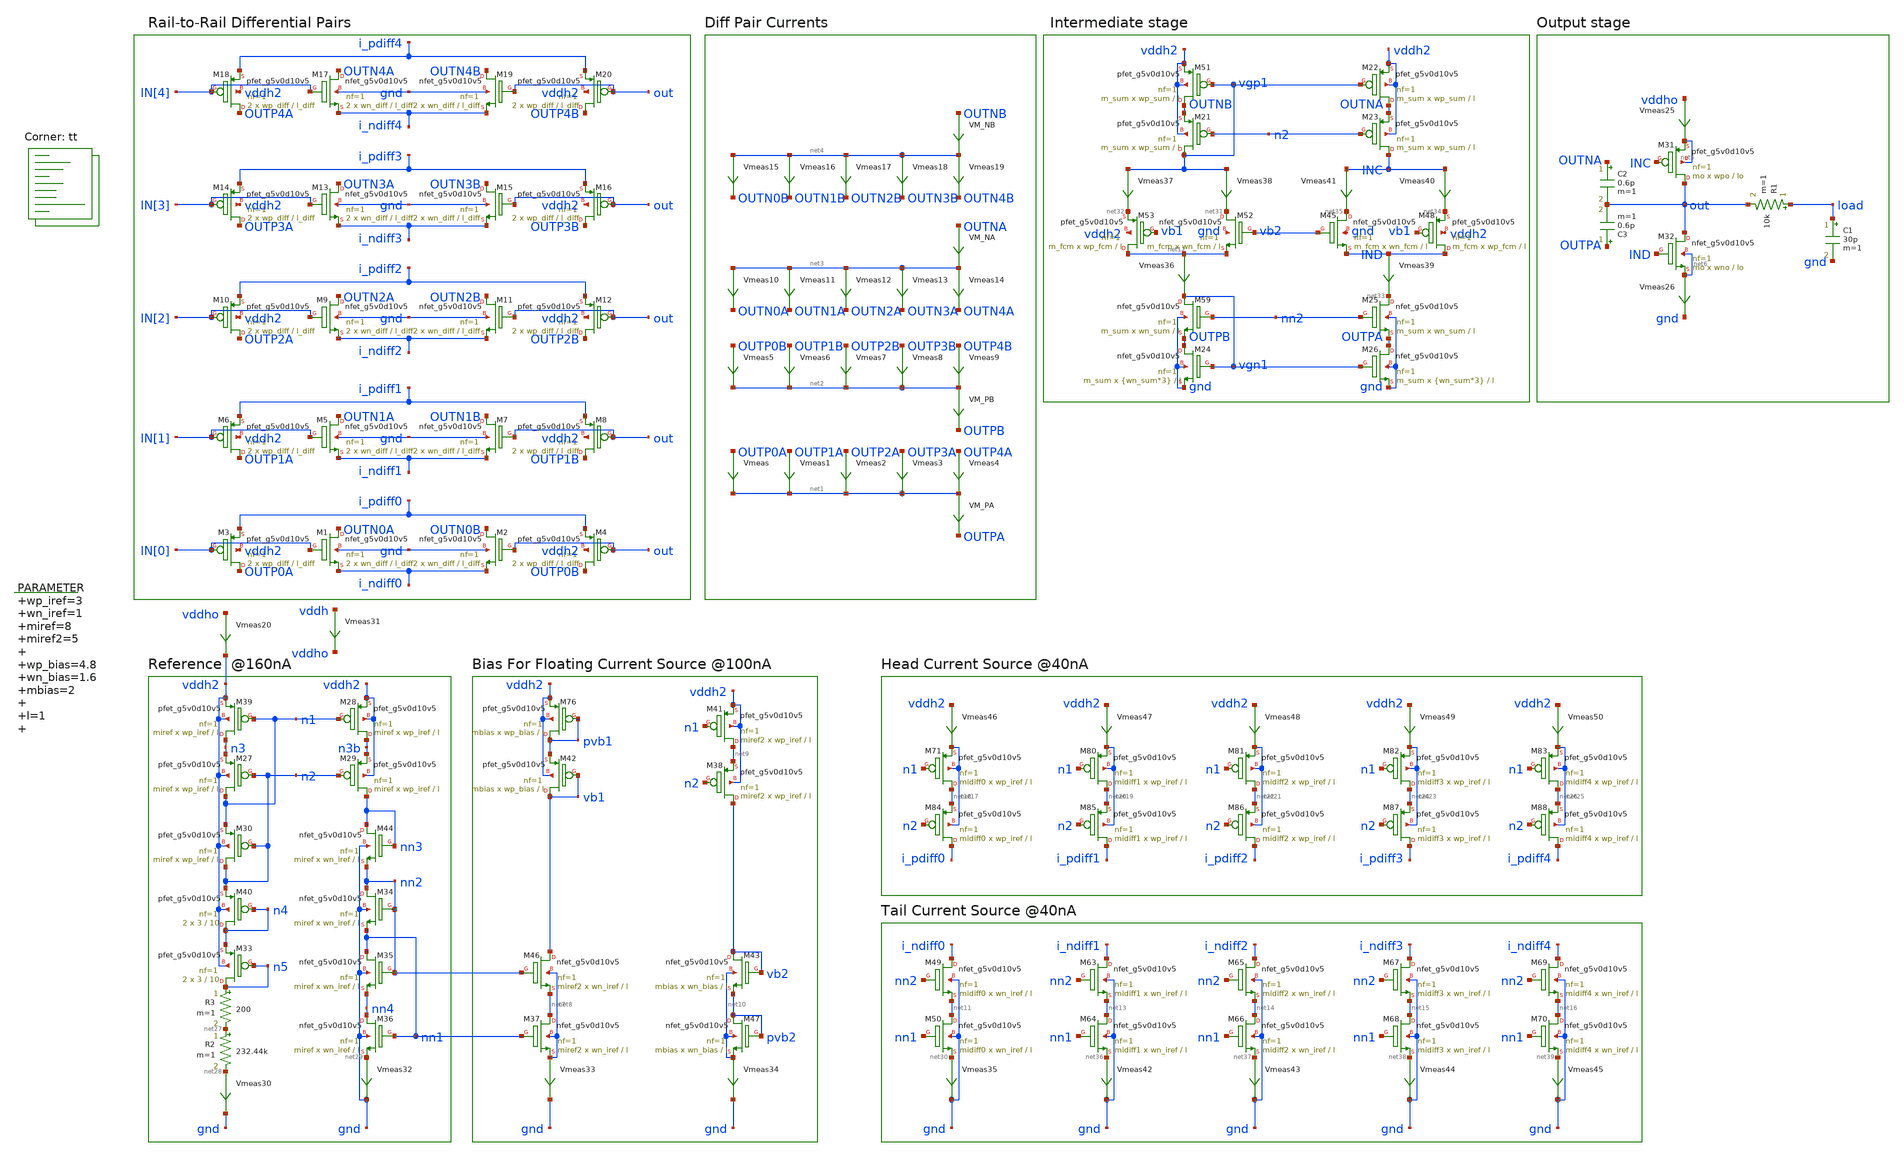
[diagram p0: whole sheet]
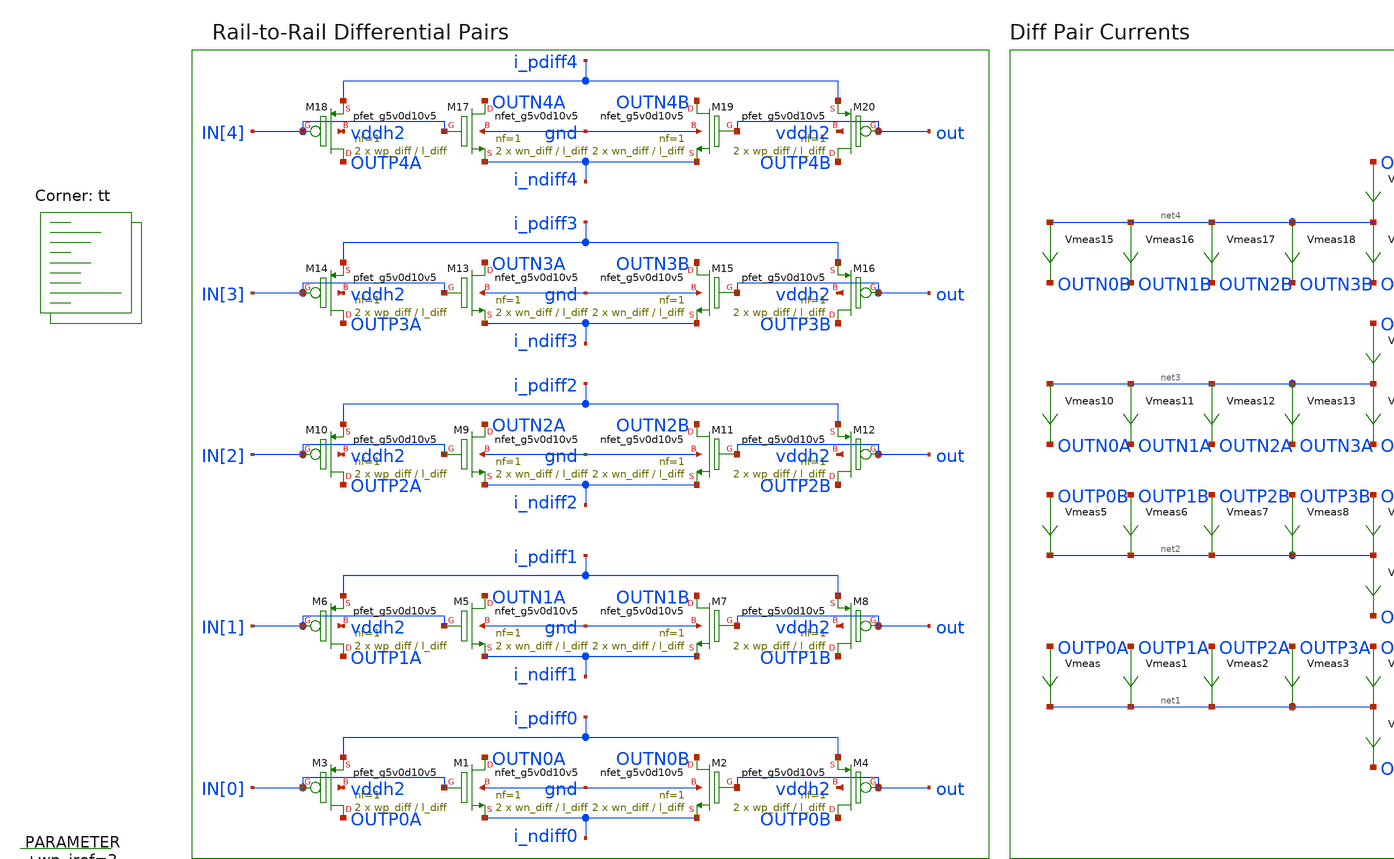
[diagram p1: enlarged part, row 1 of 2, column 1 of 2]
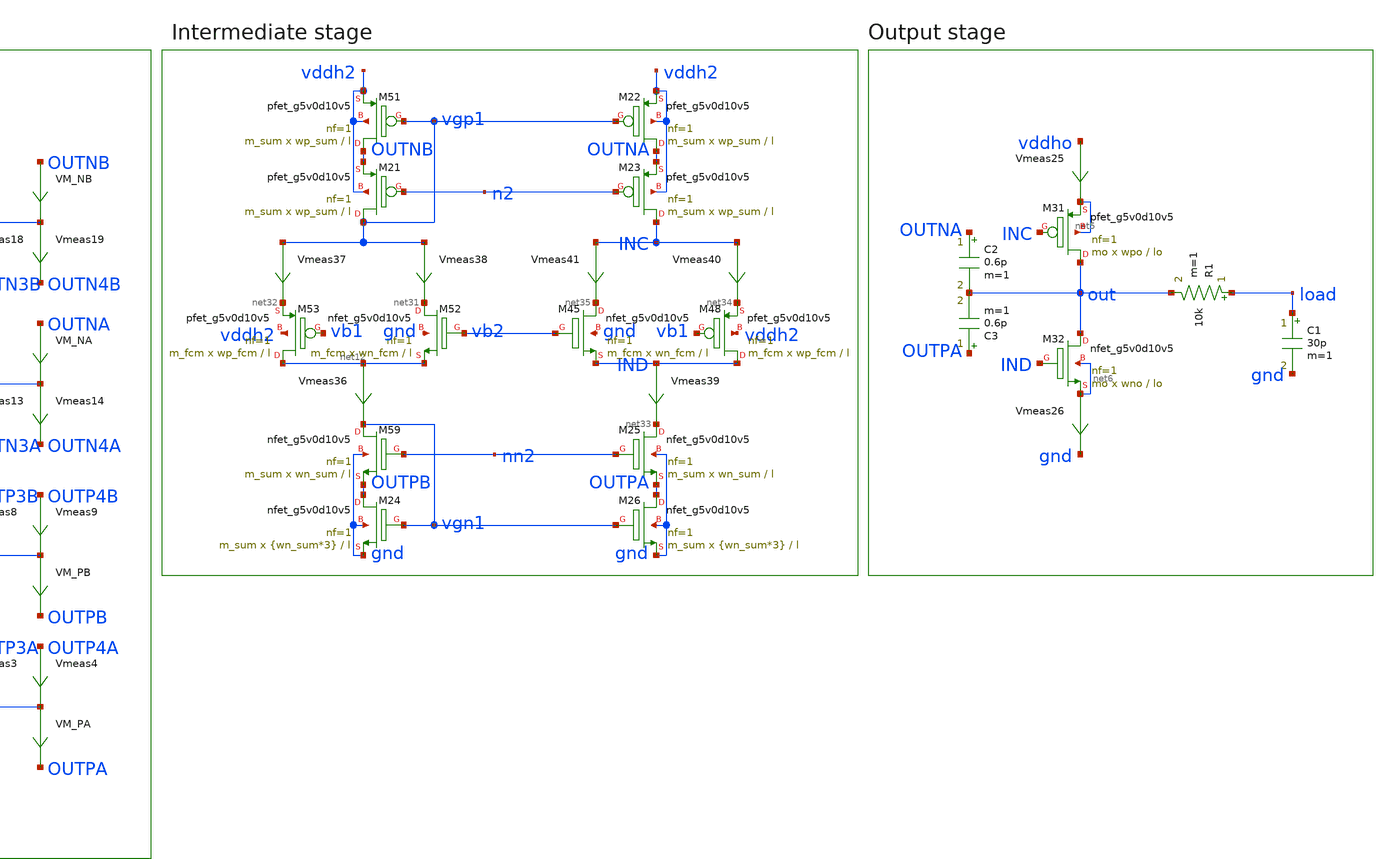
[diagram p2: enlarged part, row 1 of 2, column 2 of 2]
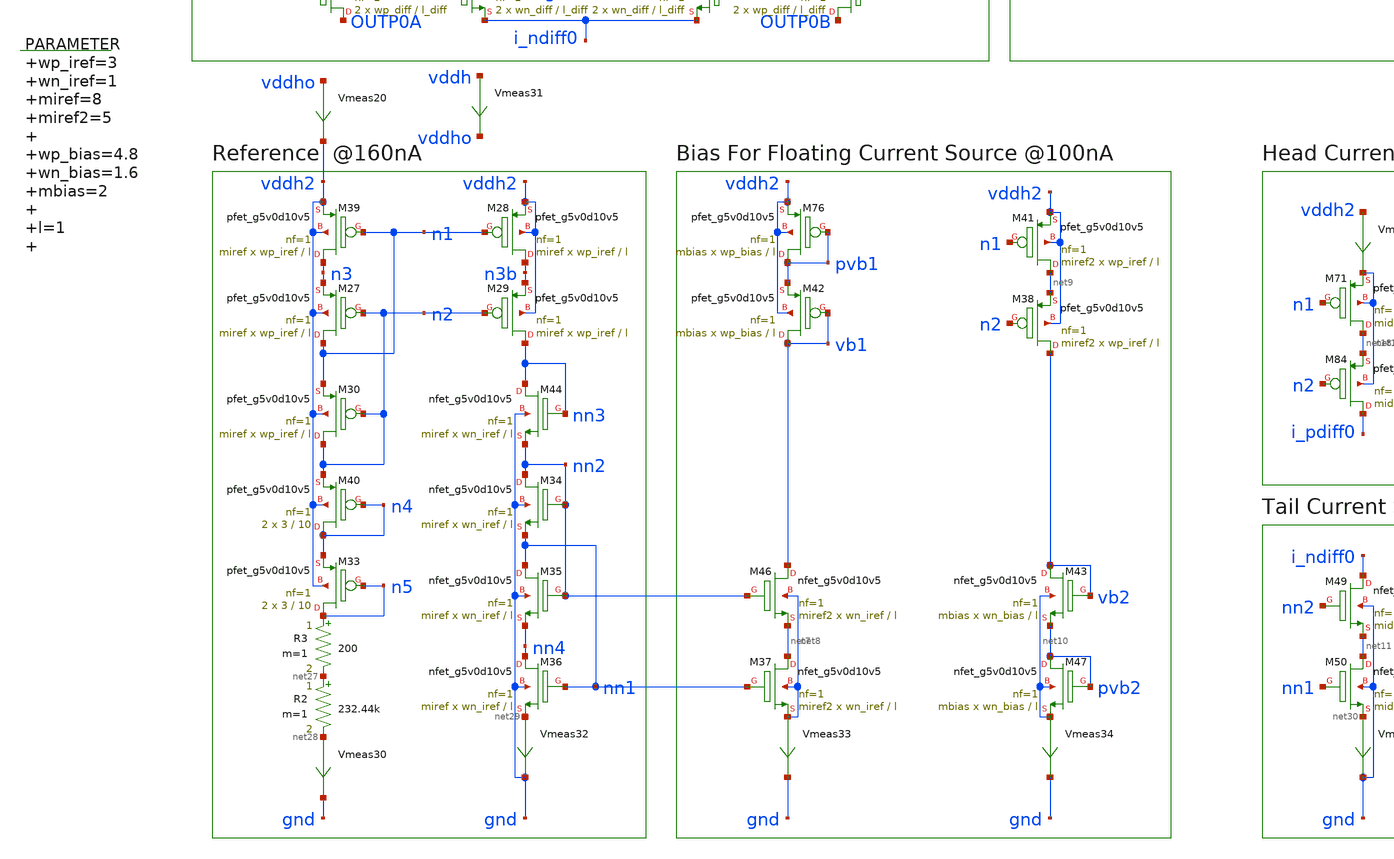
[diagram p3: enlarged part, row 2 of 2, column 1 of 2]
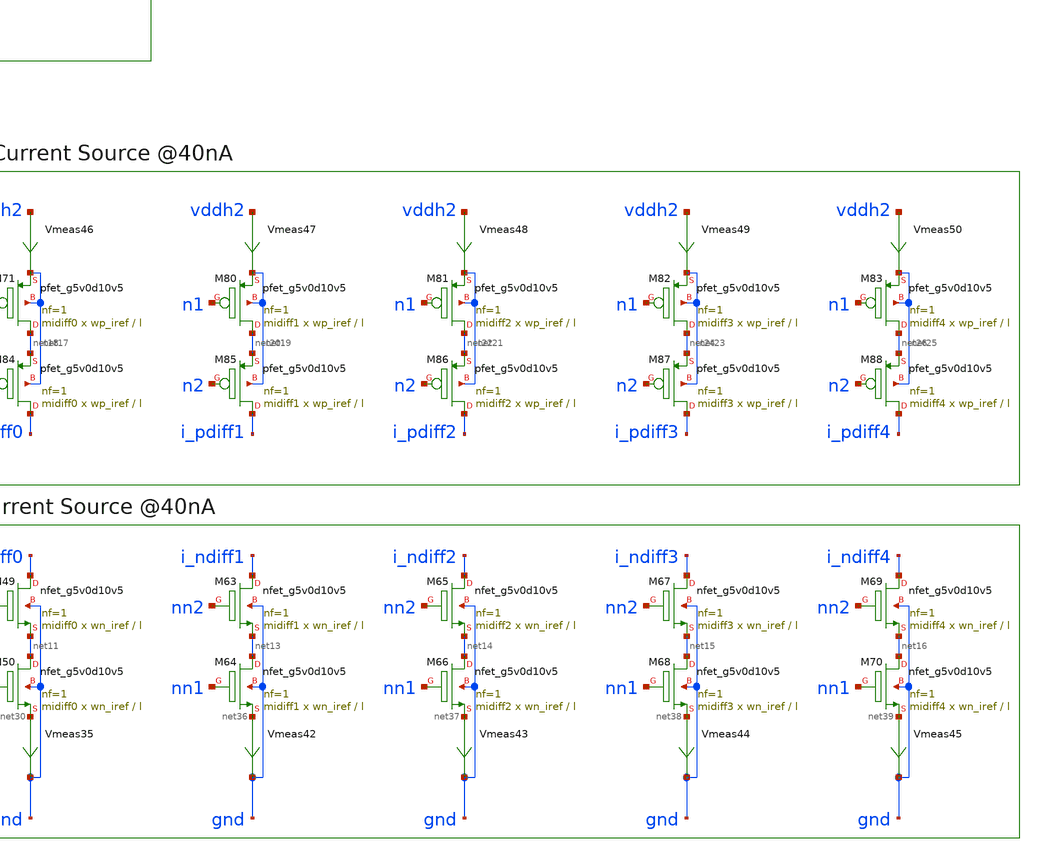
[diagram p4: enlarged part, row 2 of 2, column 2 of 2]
** sch_path: xschem/op_amp_v3-tb.sch
**.subckt op_amp_v3-tb
XM1 OUTN0A IN[0] i_ndiff0 gnd sky130_fd_pr__nfet_g5v0d10v5 L=l_diff W=wn_diff nf=1 ad='int((nf+1)/2) * W/nf * 0.29'
+ as='int((nf+2)/2) * W/nf * 0.29' pd='2*int((nf+1)/2) * (W/nf + 0.29)' ps='2*int((nf+2)/2) * (W/nf + 0.29)'
+ nrd='0.29 / W' nrs='0.29 / W' sa=0 sb=0 sd=0 mult=2 m=2
XM3 OUTP0A IN[0] i_pdiff0 vddh2 sky130_fd_pr__pfet_g5v0d10v5 L=l_diff W=wp_diff nf=1 ad='int((nf+1)/2) * W/nf * 0.29'
+ as='int((nf+2)/2) * W/nf * 0.29' pd='2*int((nf+1)/2) * (W/nf + 0.29)' ps='2*int((nf+2)/2) * (W/nf + 0.29)'
+ nrd='0.29 / W' nrs='0.29 / W' sa=0 sb=0 sd=0 mult=2 m=2
Vmeas OUTP0A net1 0
.save i(vmeas)
Vmeas1 OUTP1A net1 0
.save i(vmeas1)
Vmeas2 OUTP2A net1 0
.save i(vmeas2)
Vmeas3 OUTP3A net1 0
.save i(vmeas3)
Vmeas4 OUTP4A net1 0
.save i(vmeas4)
Vmeas5 OUTP0B net2 0
.save i(vmeas5)
Vmeas6 OUTP1B net2 0
.save i(vmeas6)
Vmeas7 OUTP2B net2 0
.save i(vmeas7)
Vmeas8 OUTP3B net2 0
.save i(vmeas8)
Vmeas9 OUTP4B net2 0
.save i(vmeas9)
Vmeas10 net3 OUTN0A 0
.save i(vmeas10)
Vmeas11 net3 OUTN1A 0
.save i(vmeas11)
Vmeas12 net3 OUTN2A 0
.save i(vmeas12)
Vmeas13 net3 OUTN3A 0
.save i(vmeas13)
Vmeas14 net3 OUTN4A 0
.save i(vmeas14)
Vmeas15 net4 OUTN0B 0
.save i(vmeas15)
Vmeas16 net4 OUTN1B 0
.save i(vmeas16)
Vmeas17 net4 OUTN2B 0
.save i(vmeas17)
Vmeas18 net4 OUTN3B 0
.save i(vmeas18)
Vmeas19 net4 OUTN4B 0
.save i(vmeas19)
XM31 out INC net5 net5 sky130_fd_pr__pfet_g5v0d10v5 L=lo W=wpo nf=1 ad='int((nf+1)/2) * W/nf * 0.29'
+ as='int((nf+2)/2) * W/nf * 0.29' pd='2*int((nf+1)/2) * (W/nf + 0.29)' ps='2*int((nf+2)/2) * (W/nf + 0.29)'
+ nrd='0.29 / W' nrs='0.29 / W' sa=0 sb=0 sd=0 mult=mo m=mo
XM32 out IND net6 net6 sky130_fd_pr__nfet_g5v0d10v5 L=lo W=wno nf=1 ad='int((nf+1)/2) * W/nf * 0.29'
+ as='int((nf+2)/2) * W/nf * 0.29' pd='2*int((nf+1)/2) * (W/nf + 0.29)' ps='2*int((nf+2)/2) * (W/nf + 0.29)'
+ nrd='0.29 / W' nrs='0.29 / W' sa=0 sb=0 sd=0 mult=mo m=mo
R1 load out 10k m=1
Vmeas25 vddho net5 0
.save i(vmeas25)
Vmeas26 net6 gnd 0
.save i(vmeas26)
C1 load gnd 30p m=1
VM_NB OUTNB net4 0
.save i(vm_nb)
VM_NA OUTNA net3 0
.save i(vm_na)
VM_PB net2 OUTPB 0
.save i(vm_pb)
VM_PA net1 OUTPA 0
.save i(vm_pa)
C2 OUTNA out 0.6p m=1
C3 OUTPA out 0.6p m=1
XM2 OUTN0B out i_ndiff0 gnd sky130_fd_pr__nfet_g5v0d10v5 L=l_diff W=wn_diff nf=1 ad='int((nf+1)/2) * W/nf * 0.29'
+ as='int((nf+2)/2) * W/nf * 0.29' pd='2*int((nf+1)/2) * (W/nf + 0.29)' ps='2*int((nf+2)/2) * (W/nf + 0.29)'
+ nrd='0.29 / W' nrs='0.29 / W' sa=0 sb=0 sd=0 mult=2 m=2
XM4 OUTP0B out i_pdiff0 vddh2 sky130_fd_pr__pfet_g5v0d10v5 L=l_diff W=wp_diff nf=1 ad='int((nf+1)/2) * W/nf * 0.29'
+ as='int((nf+2)/2) * W/nf * 0.29' pd='2*int((nf+1)/2) * (W/nf + 0.29)' ps='2*int((nf+2)/2) * (W/nf + 0.29)'
+ nrd='0.29 / W' nrs='0.29 / W' sa=0 sb=0 sd=0 mult=2 m=2
XM5 OUTN1A IN[1] i_ndiff1 gnd sky130_fd_pr__nfet_g5v0d10v5 L=l_diff W=wn_diff nf=1 ad='int((nf+1)/2) * W/nf * 0.29'
+ as='int((nf+2)/2) * W/nf * 0.29' pd='2*int((nf+1)/2) * (W/nf + 0.29)' ps='2*int((nf+2)/2) * (W/nf + 0.29)'
+ nrd='0.29 / W' nrs='0.29 / W' sa=0 sb=0 sd=0 mult=2 m=2
XM6 OUTP1A IN[1] i_pdiff1 vddh2 sky130_fd_pr__pfet_g5v0d10v5 L=l_diff W=wp_diff nf=1 ad='int((nf+1)/2) * W/nf * 0.29'
+ as='int((nf+2)/2) * W/nf * 0.29' pd='2*int((nf+1)/2) * (W/nf + 0.29)' ps='2*int((nf+2)/2) * (W/nf + 0.29)'
+ nrd='0.29 / W' nrs='0.29 / W' sa=0 sb=0 sd=0 mult=2 m=2
XM7 OUTN1B out i_ndiff1 gnd sky130_fd_pr__nfet_g5v0d10v5 L=l_diff W=wn_diff nf=1 ad='int((nf+1)/2) * W/nf * 0.29'
+ as='int((nf+2)/2) * W/nf * 0.29' pd='2*int((nf+1)/2) * (W/nf + 0.29)' ps='2*int((nf+2)/2) * (W/nf + 0.29)'
+ nrd='0.29 / W' nrs='0.29 / W' sa=0 sb=0 sd=0 mult=2 m=2
XM8 OUTP1B out i_pdiff1 vddh2 sky130_fd_pr__pfet_g5v0d10v5 L=l_diff W=wp_diff nf=1 ad='int((nf+1)/2) * W/nf * 0.29'
+ as='int((nf+2)/2) * W/nf * 0.29' pd='2*int((nf+1)/2) * (W/nf + 0.29)' ps='2*int((nf+2)/2) * (W/nf + 0.29)'
+ nrd='0.29 / W' nrs='0.29 / W' sa=0 sb=0 sd=0 mult=2 m=2
XM9 OUTN2A IN[2] i_ndiff2 gnd sky130_fd_pr__nfet_g5v0d10v5 L=l_diff W=wn_diff nf=1 ad='int((nf+1)/2) * W/nf * 0.29'
+ as='int((nf+2)/2) * W/nf * 0.29' pd='2*int((nf+1)/2) * (W/nf + 0.29)' ps='2*int((nf+2)/2) * (W/nf + 0.29)'
+ nrd='0.29 / W' nrs='0.29 / W' sa=0 sb=0 sd=0 mult=2 m=2
XM10 OUTP2A IN[2] i_pdiff2 vddh2 sky130_fd_pr__pfet_g5v0d10v5 L=l_diff W=wp_diff nf=1 ad='int((nf+1)/2) * W/nf * 0.29'
+ as='int((nf+2)/2) * W/nf * 0.29' pd='2*int((nf+1)/2) * (W/nf + 0.29)' ps='2*int((nf+2)/2) * (W/nf + 0.29)'
+ nrd='0.29 / W' nrs='0.29 / W' sa=0 sb=0 sd=0 mult=2 m=2
XM11 OUTN2B out i_ndiff2 gnd sky130_fd_pr__nfet_g5v0d10v5 L=l_diff W=wn_diff nf=1 ad='int((nf+1)/2) * W/nf * 0.29'
+ as='int((nf+2)/2) * W/nf * 0.29' pd='2*int((nf+1)/2) * (W/nf + 0.29)' ps='2*int((nf+2)/2) * (W/nf + 0.29)'
+ nrd='0.29 / W' nrs='0.29 / W' sa=0 sb=0 sd=0 mult=2 m=2
XM12 OUTP2B out i_pdiff2 vddh2 sky130_fd_pr__pfet_g5v0d10v5 L=l_diff W=wp_diff nf=1 ad='int((nf+1)/2) * W/nf * 0.29'
+ as='int((nf+2)/2) * W/nf * 0.29' pd='2*int((nf+1)/2) * (W/nf + 0.29)' ps='2*int((nf+2)/2) * (W/nf + 0.29)'
+ nrd='0.29 / W' nrs='0.29 / W' sa=0 sb=0 sd=0 mult=2 m=2
XM13 OUTN3A IN[3] i_ndiff3 gnd sky130_fd_pr__nfet_g5v0d10v5 L=l_diff W=wn_diff nf=1 ad='int((nf+1)/2) * W/nf * 0.29'
+ as='int((nf+2)/2) * W/nf * 0.29' pd='2*int((nf+1)/2) * (W/nf + 0.29)' ps='2*int((nf+2)/2) * (W/nf + 0.29)'
+ nrd='0.29 / W' nrs='0.29 / W' sa=0 sb=0 sd=0 mult=2 m=2
XM14 OUTP3A IN[3] i_pdiff3 vddh2 sky130_fd_pr__pfet_g5v0d10v5 L=l_diff W=wp_diff nf=1 ad='int((nf+1)/2) * W/nf * 0.29'
+ as='int((nf+2)/2) * W/nf * 0.29' pd='2*int((nf+1)/2) * (W/nf + 0.29)' ps='2*int((nf+2)/2) * (W/nf + 0.29)'
+ nrd='0.29 / W' nrs='0.29 / W' sa=0 sb=0 sd=0 mult=2 m=2
XM15 OUTN3B out i_ndiff3 gnd sky130_fd_pr__nfet_g5v0d10v5 L=l_diff W=wn_diff nf=1 ad='int((nf+1)/2) * W/nf * 0.29'
+ as='int((nf+2)/2) * W/nf * 0.29' pd='2*int((nf+1)/2) * (W/nf + 0.29)' ps='2*int((nf+2)/2) * (W/nf + 0.29)'
+ nrd='0.29 / W' nrs='0.29 / W' sa=0 sb=0 sd=0 mult=2 m=2
XM16 OUTP3B out i_pdiff3 vddh2 sky130_fd_pr__pfet_g5v0d10v5 L=l_diff W=wp_diff nf=1 ad='int((nf+1)/2) * W/nf * 0.29'
+ as='int((nf+2)/2) * W/nf * 0.29' pd='2*int((nf+1)/2) * (W/nf + 0.29)' ps='2*int((nf+2)/2) * (W/nf + 0.29)'
+ nrd='0.29 / W' nrs='0.29 / W' sa=0 sb=0 sd=0 mult=2 m=2
XM17 OUTN4A IN[4] i_ndiff4 gnd sky130_fd_pr__nfet_g5v0d10v5 L=l_diff W=wn_diff nf=1 ad='int((nf+1)/2) * W/nf * 0.29'
+ as='int((nf+2)/2) * W/nf * 0.29' pd='2*int((nf+1)/2) * (W/nf + 0.29)' ps='2*int((nf+2)/2) * (W/nf + 0.29)'
+ nrd='0.29 / W' nrs='0.29 / W' sa=0 sb=0 sd=0 mult=2 m=2
XM18 OUTP4A IN[4] i_pdiff4 vddh2 sky130_fd_pr__pfet_g5v0d10v5 L=l_diff W=wp_diff nf=1 ad='int((nf+1)/2) * W/nf * 0.29'
+ as='int((nf+2)/2) * W/nf * 0.29' pd='2*int((nf+1)/2) * (W/nf + 0.29)' ps='2*int((nf+2)/2) * (W/nf + 0.29)'
+ nrd='0.29 / W' nrs='0.29 / W' sa=0 sb=0 sd=0 mult=2 m=2
XM19 OUTN4B out i_ndiff4 gnd sky130_fd_pr__nfet_g5v0d10v5 L=l_diff W=wn_diff nf=1 ad='int((nf+1)/2) * W/nf * 0.29'
+ as='int((nf+2)/2) * W/nf * 0.29' pd='2*int((nf+1)/2) * (W/nf + 0.29)' ps='2*int((nf+2)/2) * (W/nf + 0.29)'
+ nrd='0.29 / W' nrs='0.29 / W' sa=0 sb=0 sd=0 mult=2 m=2
XM20 OUTP4B out i_pdiff4 vddh2 sky130_fd_pr__pfet_g5v0d10v5 L=l_diff W=wp_diff nf=1 ad='int((nf+1)/2) * W/nf * 0.29'
+ as='int((nf+2)/2) * W/nf * 0.29' pd='2*int((nf+1)/2) * (W/nf + 0.29)' ps='2*int((nf+2)/2) * (W/nf + 0.29)'
+ nrd='0.29 / W' nrs='0.29 / W' sa=0 sb=0 sd=0 mult=2 m=2
XM39 n3 n1 vddh2 vddh2 sky130_fd_pr__pfet_g5v0d10v5 L=l W=wp_iref nf=1 ad='int((nf+1)/2) * W/nf * 0.29'
+ as='int((nf+2)/2) * W/nf * 0.29' pd='2*int((nf+1)/2) * (W/nf + 0.29)' ps='2*int((nf+2)/2) * (W/nf + 0.29)'
+ nrd='0.29 / W' nrs='0.29 / W' sa=0 sb=0 sd=0 mult=miref m=miref
R2 net27 net28 232.44k m=1
Vmeas30 net28 gnd 0
.save i(vmeas30)
R3 n5 net27 200 m=1
XM40 n4 n4 n2 vddh2 sky130_fd_pr__pfet_g5v0d10v5 L=10 W=3 nf=1 ad='int((nf+1)/2) * W/nf * 0.29' as='int((nf+2)/2) * W/nf * 0.29'
+ pd='2*int((nf+1)/2) * (W/nf + 0.29)' ps='2*int((nf+2)/2) * (W/nf + 0.29)' nrd='0.29 / W' nrs='0.29 / W'
+ sa=0 sb=0 sd=0 mult=2 m=2
Vmeas31 vddh vddho 0
.save i(vmeas31)
XM44 nn3 nn3 nn2 gnd sky130_fd_pr__nfet_g5v0d10v5 L=l W=wn_iref nf=1 ad='int((nf+1)/2) * W/nf * 0.29'
+ as='int((nf+2)/2) * W/nf * 0.29' pd='2*int((nf+1)/2) * (W/nf + 0.29)' ps='2*int((nf+2)/2) * (W/nf + 0.29)'
+ nrd='0.29 / W' nrs='0.29 / W' sa=0 sb=0 sd=0 mult=miref m=miref
Vmeas32 net29 gnd 0
.save i(vmeas32)
XM46 vb1 nn2 net7 net8 sky130_fd_pr__nfet_g5v0d10v5 L=l W=wn_iref nf=1 ad='int((nf+1)/2) * W/nf * 0.29'
+ as='int((nf+2)/2) * W/nf * 0.29' pd='2*int((nf+1)/2) * (W/nf + 0.29)' ps='2*int((nf+2)/2) * (W/nf + 0.29)'
+ nrd='0.29 / W' nrs='0.29 / W' sa=0 sb=0 sd=0 mult=miref2 m=miref2
Vmeas33 net8 gnd 0
.save i(vmeas33)
XM47 pvb2 pvb2 net10 net10 sky130_fd_pr__nfet_g5v0d10v5 L=l W=wn_bias nf=1 ad='int((nf+1)/2) * W/nf * 0.29'
+ as='int((nf+2)/2) * W/nf * 0.29' pd='2*int((nf+1)/2) * (W/nf + 0.29)' ps='2*int((nf+2)/2) * (W/nf + 0.29)'
+ nrd='0.29 / W' nrs='0.29 / W' sa=0 sb=0 sd=0 mult=mbias m=mbias
Vmeas34 net10 gnd 0
.save i(vmeas34)
XM49 i_ndiff0 nn2 net11 gnd sky130_fd_pr__nfet_g5v0d10v5 L=l W=wn_iref nf=1 ad='int((nf+1)/2) * W/nf * 0.29'
+ as='int((nf+2)/2) * W/nf * 0.29' pd='2*int((nf+1)/2) * (W/nf + 0.29)' ps='2*int((nf+2)/2) * (W/nf + 0.29)'
+ nrd='0.29 / W' nrs='0.29 / W' sa=0 sb=0 sd=0 mult=midiff0 m=midiff0
XM50 net11 nn1 net30 gnd sky130_fd_pr__nfet_g5v0d10v5 L=l W=wn_iref nf=1 ad='int((nf+1)/2) * W/nf * 0.29'
+ as='int((nf+2)/2) * W/nf * 0.29' pd='2*int((nf+1)/2) * (W/nf + 0.29)' ps='2*int((nf+2)/2) * (W/nf + 0.29)'
+ nrd='0.29 / W' nrs='0.29 / W' sa=0 sb=0 sd=0 mult=midiff0 m=midiff0
Vmeas35 net30 gnd 0
.save i(vmeas35)
Vmeas36 net12 vgn1 0
.save i(vmeas36)
XM51 OUTNB vgp1 vddh2 vddh2 sky130_fd_pr__pfet_g5v0d10v5 L=l W=wp_sum nf=1 ad='int((nf+1)/2) * W/nf * 0.29'
+ as='int((nf+2)/2) * W/nf * 0.29' pd='2*int((nf+1)/2) * (W/nf + 0.29)' ps='2*int((nf+2)/2) * (W/nf + 0.29)'
+ nrd='0.29 / W' nrs='0.29 / W' sa=0 sb=0 sd=0 mult=m_sum m=m_sum
XM52 net31 vb2 net12 gnd sky130_fd_pr__nfet_g5v0d10v5 L=l W=wn_fcm nf=1 ad='int((nf+1)/2) * W/nf * 0.29'
+ as='int((nf+2)/2) * W/nf * 0.29' pd='2*int((nf+1)/2) * (W/nf + 0.29)' ps='2*int((nf+2)/2) * (W/nf + 0.29)'
+ nrd='0.29 / W' nrs='0.29 / W' sa=0 sb=0 sd=0 mult=m_fcm m=m_fcm
Vmeas37 vgp1 net32 0
.save i(vmeas37)
Vmeas38 vgp1 net31 0
.save i(vmeas38)
XM53 net12 vb1 net32 vddh2 sky130_fd_pr__pfet_g5v0d10v5 L=l W=wp_fcm nf=1 ad='int((nf+1)/2) * W/nf * 0.29'
+ as='int((nf+2)/2) * W/nf * 0.29' pd='2*int((nf+1)/2) * (W/nf + 0.29)' ps='2*int((nf+2)/2) * (W/nf + 0.29)'
+ nrd='0.29 / W' nrs='0.29 / W' sa=0 sb=0 sd=0 mult=m_fcm m=m_fcm
Vmeas39 IND net33 0
.save i(vmeas39)
Vmeas40 INC net34 0
.save i(vmeas40)
Vmeas41 INC net35 0
.save i(vmeas41)
XM59 vgn1 nn2 OUTPB gnd sky130_fd_pr__nfet_g5v0d10v5 L=l W=wn_sum nf=1 ad='int((nf+1)/2) * W/nf * 0.29'
+ as='int((nf+2)/2) * W/nf * 0.29' pd='2*int((nf+1)/2) * (W/nf + 0.29)' ps='2*int((nf+2)/2) * (W/nf + 0.29)'
+ nrd='0.29 / W' nrs='0.29 / W' sa=0 sb=0 sd=0 mult=m_sum m=m_sum
XM63 i_ndiff1 nn2 net13 gnd sky130_fd_pr__nfet_g5v0d10v5 L=l W=wn_iref nf=1 ad='int((nf+1)/2) * W/nf * 0.29'
+ as='int((nf+2)/2) * W/nf * 0.29' pd='2*int((nf+1)/2) * (W/nf + 0.29)' ps='2*int((nf+2)/2) * (W/nf + 0.29)'
+ nrd='0.29 / W' nrs='0.29 / W' sa=0 sb=0 sd=0 mult=midiff1 m=midiff1
XM64 net13 nn1 net36 gnd sky130_fd_pr__nfet_g5v0d10v5 L=l W=wn_iref nf=1 ad='int((nf+1)/2) * W/nf * 0.29'
+ as='int((nf+2)/2) * W/nf * 0.29' pd='2*int((nf+1)/2) * (W/nf + 0.29)' ps='2*int((nf+2)/2) * (W/nf + 0.29)'
+ nrd='0.29 / W' nrs='0.29 / W' sa=0 sb=0 sd=0 mult=midiff1 m=midiff1
Vmeas42 net36 gnd 0
.save i(vmeas42)
XM65 i_ndiff2 nn2 net14 gnd sky130_fd_pr__nfet_g5v0d10v5 L=l W=wn_iref nf=1 ad='int((nf+1)/2) * W/nf * 0.29'
+ as='int((nf+2)/2) * W/nf * 0.29' pd='2*int((nf+1)/2) * (W/nf + 0.29)' ps='2*int((nf+2)/2) * (W/nf + 0.29)'
+ nrd='0.29 / W' nrs='0.29 / W' sa=0 sb=0 sd=0 mult=midiff2 m=midiff2
XM66 net14 nn1 net37 gnd sky130_fd_pr__nfet_g5v0d10v5 L=l W=wn_iref nf=1 ad='int((nf+1)/2) * W/nf * 0.29'
+ as='int((nf+2)/2) * W/nf * 0.29' pd='2*int((nf+1)/2) * (W/nf + 0.29)' ps='2*int((nf+2)/2) * (W/nf + 0.29)'
+ nrd='0.29 / W' nrs='0.29 / W' sa=0 sb=0 sd=0 mult=midiff2 m=midiff2
Vmeas43 net37 gnd 0
.save i(vmeas43)
XM67 i_ndiff3 nn2 net15 gnd sky130_fd_pr__nfet_g5v0d10v5 L=l W=wn_iref nf=1 ad='int((nf+1)/2) * W/nf * 0.29'
+ as='int((nf+2)/2) * W/nf * 0.29' pd='2*int((nf+1)/2) * (W/nf + 0.29)' ps='2*int((nf+2)/2) * (W/nf + 0.29)'
+ nrd='0.29 / W' nrs='0.29 / W' sa=0 sb=0 sd=0 mult=midiff3 m=midiff3
XM68 net15 nn1 net38 gnd sky130_fd_pr__nfet_g5v0d10v5 L=l W=wn_iref nf=1 ad='int((nf+1)/2) * W/nf * 0.29'
+ as='int((nf+2)/2) * W/nf * 0.29' pd='2*int((nf+1)/2) * (W/nf + 0.29)' ps='2*int((nf+2)/2) * (W/nf + 0.29)'
+ nrd='0.29 / W' nrs='0.29 / W' sa=0 sb=0 sd=0 mult=midiff3 m=midiff3
Vmeas44 net38 gnd 0
.save i(vmeas44)
XM69 i_ndiff4 nn2 net16 gnd sky130_fd_pr__nfet_g5v0d10v5 L=l W=wn_iref nf=1 ad='int((nf+1)/2) * W/nf * 0.29'
+ as='int((nf+2)/2) * W/nf * 0.29' pd='2*int((nf+1)/2) * (W/nf + 0.29)' ps='2*int((nf+2)/2) * (W/nf + 0.29)'
+ nrd='0.29 / W' nrs='0.29 / W' sa=0 sb=0 sd=0 mult=midiff4 m=midiff4
XM70 net16 nn1 net39 gnd sky130_fd_pr__nfet_g5v0d10v5 L=l W=wn_iref nf=1 ad='int((nf+1)/2) * W/nf * 0.29'
+ as='int((nf+2)/2) * W/nf * 0.29' pd='2*int((nf+1)/2) * (W/nf + 0.29)' ps='2*int((nf+2)/2) * (W/nf + 0.29)'
+ nrd='0.29 / W' nrs='0.29 / W' sa=0 sb=0 sd=0 mult=midiff4 m=midiff4
Vmeas45 net39 gnd 0
.save i(vmeas45)
XM71 net18 n1 net17 net17 sky130_fd_pr__pfet_g5v0d10v5 L=l W=wp_iref nf=1 ad='int((nf+1)/2) * W/nf * 0.29'
+ as='int((nf+2)/2) * W/nf * 0.29' pd='2*int((nf+1)/2) * (W/nf + 0.29)' ps='2*int((nf+2)/2) * (W/nf + 0.29)'
+ nrd='0.29 / W' nrs='0.29 / W' sa=0 sb=0 sd=0 mult=midiff0 m=midiff0
Vmeas46 vddh2 net17 0
.save i(vmeas46)
XM76 pvb1 pvb1 vddh2 vddh2 sky130_fd_pr__pfet_g5v0d10v5 L=l W=wp_bias nf=1 ad='int((nf+1)/2) * W/nf * 0.29'
+ as='int((nf+2)/2) * W/nf * 0.29' pd='2*int((nf+1)/2) * (W/nf + 0.29)' ps='2*int((nf+2)/2) * (W/nf + 0.29)'
+ nrd='0.29 / W' nrs='0.29 / W' sa=0 sb=0 sd=0 mult=mbias m=mbias
XM80 net20 n1 net19 net19 sky130_fd_pr__pfet_g5v0d10v5 L=l W=wp_iref nf=1 ad='int((nf+1)/2) * W/nf * 0.29'
+ as='int((nf+2)/2) * W/nf * 0.29' pd='2*int((nf+1)/2) * (W/nf + 0.29)' ps='2*int((nf+2)/2) * (W/nf + 0.29)'
+ nrd='0.29 / W' nrs='0.29 / W' sa=0 sb=0 sd=0 mult=midiff1 m=midiff1
Vmeas47 vddh2 net19 0
.save i(vmeas47)
XM81 net22 n1 net21 net21 sky130_fd_pr__pfet_g5v0d10v5 L=l W=wp_iref nf=1 ad='int((nf+1)/2) * W/nf * 0.29'
+ as='int((nf+2)/2) * W/nf * 0.29' pd='2*int((nf+1)/2) * (W/nf + 0.29)' ps='2*int((nf+2)/2) * (W/nf + 0.29)'
+ nrd='0.29 / W' nrs='0.29 / W' sa=0 sb=0 sd=0 mult=midiff2 m=midiff2
Vmeas48 vddh2 net21 0
.save i(vmeas48)
XM82 net24 n1 net23 net23 sky130_fd_pr__pfet_g5v0d10v5 L=l W=wp_iref nf=1 ad='int((nf+1)/2) * W/nf * 0.29'
+ as='int((nf+2)/2) * W/nf * 0.29' pd='2*int((nf+1)/2) * (W/nf + 0.29)' ps='2*int((nf+2)/2) * (W/nf + 0.29)'
+ nrd='0.29 / W' nrs='0.29 / W' sa=0 sb=0 sd=0 mult=midiff3 m=midiff3
Vmeas49 vddh2 net23 0
.save i(vmeas49)
XM83 net26 n1 net25 net25 sky130_fd_pr__pfet_g5v0d10v5 L=l W=wp_iref nf=1 ad='int((nf+1)/2) * W/nf * 0.29'
+ as='int((nf+2)/2) * W/nf * 0.29' pd='2*int((nf+1)/2) * (W/nf + 0.29)' ps='2*int((nf+2)/2) * (W/nf + 0.29)'
+ nrd='0.29 / W' nrs='0.29 / W' sa=0 sb=0 sd=0 mult=midiff4 m=midiff4
Vmeas50 vddh2 net25 0
.save i(vmeas50)
XM84 i_pdiff0 n2 net18 net17 sky130_fd_pr__pfet_g5v0d10v5 L=l W=wp_iref nf=1 ad='int((nf+1)/2) * W/nf * 0.29'
+ as='int((nf+2)/2) * W/nf * 0.29' pd='2*int((nf+1)/2) * (W/nf + 0.29)' ps='2*int((nf+2)/2) * (W/nf + 0.29)'
+ nrd='0.29 / W' nrs='0.29 / W' sa=0 sb=0 sd=0 mult=midiff0 m=midiff0
XM85 i_pdiff1 n2 net20 net19 sky130_fd_pr__pfet_g5v0d10v5 L=l W=wp_iref nf=1 ad='int((nf+1)/2) * W/nf * 0.29'
+ as='int((nf+2)/2) * W/nf * 0.29' pd='2*int((nf+1)/2) * (W/nf + 0.29)' ps='2*int((nf+2)/2) * (W/nf + 0.29)'
+ nrd='0.29 / W' nrs='0.29 / W' sa=0 sb=0 sd=0 mult=midiff1 m=midiff1
XM86 i_pdiff2 n2 net22 net21 sky130_fd_pr__pfet_g5v0d10v5 L=l W=wp_iref nf=1 ad='int((nf+1)/2) * W/nf * 0.29'
+ as='int((nf+2)/2) * W/nf * 0.29' pd='2*int((nf+1)/2) * (W/nf + 0.29)' ps='2*int((nf+2)/2) * (W/nf + 0.29)'
+ nrd='0.29 / W' nrs='0.29 / W' sa=0 sb=0 sd=0 mult=midiff2 m=midiff2
XM87 i_pdiff3 n2 net24 net23 sky130_fd_pr__pfet_g5v0d10v5 L=l W=wp_iref nf=1 ad='int((nf+1)/2) * W/nf * 0.29'
+ as='int((nf+2)/2) * W/nf * 0.29' pd='2*int((nf+1)/2) * (W/nf + 0.29)' ps='2*int((nf+2)/2) * (W/nf + 0.29)'
+ nrd='0.29 / W' nrs='0.29 / W' sa=0 sb=0 sd=0 mult=midiff3 m=midiff3
XM88 i_pdiff4 n2 net26 net25 sky130_fd_pr__pfet_g5v0d10v5 L=l W=wp_iref nf=1 ad='int((nf+1)/2) * W/nf * 0.29'
+ as='int((nf+2)/2) * W/nf * 0.29' pd='2*int((nf+1)/2) * (W/nf + 0.29)' ps='2*int((nf+2)/2) * (W/nf + 0.29)'
+ nrd='0.29 / W' nrs='0.29 / W' sa=0 sb=0 sd=0 mult=midiff4 m=midiff4
.param wp_iref=3 wn_iref=1 miref=8 miref2=5 wp_bias=4.8 wn_bias=1.6 mbias=2 l=1 midiff0=2 midiff1=2 midiff2=4
+ midiff3=8 midiff4=16 wp_diff=3 wn_diff=1 l_diff=1 wp_sum=4.8 wn_sum=1.6 l_sum=1 m_sum=2 wp_fcm={wp_bias}
+ wn_fcm={wn_bias} m_fcm=2 wpo=9 wno=3 lo=1 mo=2

XM21 vgp1 n2 OUTNB vddh2 sky130_fd_pr__pfet_g5v0d10v5 L=l W=wp_sum nf=1 ad='int((nf+1)/2) * W/nf * 0.29'
+ as='int((nf+2)/2) * W/nf * 0.29' pd='2*int((nf+1)/2) * (W/nf + 0.29)' ps='2*int((nf+2)/2) * (W/nf + 0.29)'
+ nrd='0.29 / W' nrs='0.29 / W' sa=0 sb=0 sd=0 mult=m_sum m=m_sum
XM22 OUTNA vgp1 vddh2 vddh2 sky130_fd_pr__pfet_g5v0d10v5 L=l W=wp_sum nf=1 ad='int((nf+1)/2) * W/nf * 0.29'
+ as='int((nf+2)/2) * W/nf * 0.29' pd='2*int((nf+1)/2) * (W/nf + 0.29)' ps='2*int((nf+2)/2) * (W/nf + 0.29)'
+ nrd='0.29 / W' nrs='0.29 / W' sa=0 sb=0 sd=0 mult=m_sum m=m_sum
XM23 INC n2 OUTNA vddh2 sky130_fd_pr__pfet_g5v0d10v5 L=l W=wp_sum nf=1 ad='int((nf+1)/2) * W/nf * 0.29'
+ as='int((nf+2)/2) * W/nf * 0.29' pd='2*int((nf+1)/2) * (W/nf + 0.29)' ps='2*int((nf+2)/2) * (W/nf + 0.29)'
+ nrd='0.29 / W' nrs='0.29 / W' sa=0 sb=0 sd=0 mult=m_sum m=m_sum
XM24 OUTPB vgn1 gnd gnd sky130_fd_pr__nfet_g5v0d10v5 L=l W={wn_sum*3} nf=1 ad='int((nf+1)/2) * W/nf * 0.29'
+ as='int((nf+2)/2) * W/nf * 0.29' pd='2*int((nf+1)/2) * (W/nf + 0.29)' ps='2*int((nf+2)/2) * (W/nf + 0.29)'
+ nrd='0.29 / W' nrs='0.29 / W' sa=0 sb=0 sd=0 mult=m_sum m=m_sum
XM25 net33 nn2 OUTPA gnd sky130_fd_pr__nfet_g5v0d10v5 L=l W=wn_sum nf=1 ad='int((nf+1)/2) * W/nf * 0.29'
+ as='int((nf+2)/2) * W/nf * 0.29' pd='2*int((nf+1)/2) * (W/nf + 0.29)' ps='2*int((nf+2)/2) * (W/nf + 0.29)'
+ nrd='0.29 / W' nrs='0.29 / W' sa=0 sb=0 sd=0 mult=m_sum m=m_sum
Vmeas20 vddho vddh2 0
.save i(vmeas20)
XM27 n1 n2 n3 vddh2 sky130_fd_pr__pfet_g5v0d10v5 L=l W=wp_iref nf=1 ad='int((nf+1)/2) * W/nf * 0.29'
+ as='int((nf+2)/2) * W/nf * 0.29' pd='2*int((nf+1)/2) * (W/nf + 0.29)' ps='2*int((nf+2)/2) * (W/nf + 0.29)'
+ nrd='0.29 / W' nrs='0.29 / W' sa=0 sb=0 sd=0 mult=miref m=miref
XM28 n3b n1 vddh2 vddh2 sky130_fd_pr__pfet_g5v0d10v5 L=l W=wp_iref nf=1 ad='int((nf+1)/2) * W/nf * 0.29'
+ as='int((nf+2)/2) * W/nf * 0.29' pd='2*int((nf+1)/2) * (W/nf + 0.29)' ps='2*int((nf+2)/2) * (W/nf + 0.29)'
+ nrd='0.29 / W' nrs='0.29 / W' sa=0 sb=0 sd=0 mult=miref m=miref
XM29 nn3 n2 n3b vddh2 sky130_fd_pr__pfet_g5v0d10v5 L=l W=wp_iref nf=1 ad='int((nf+1)/2) * W/nf * 0.29'
+ as='int((nf+2)/2) * W/nf * 0.29' pd='2*int((nf+1)/2) * (W/nf + 0.29)' ps='2*int((nf+2)/2) * (W/nf + 0.29)'
+ nrd='0.29 / W' nrs='0.29 / W' sa=0 sb=0 sd=0 mult=miref m=miref
XM30 n2 n2 n1 vddh2 sky130_fd_pr__pfet_g5v0d10v5 L=l W=wp_iref nf=1 ad='int((nf+1)/2) * W/nf * 0.29'
+ as='int((nf+2)/2) * W/nf * 0.29' pd='2*int((nf+1)/2) * (W/nf + 0.29)' ps='2*int((nf+2)/2) * (W/nf + 0.29)'
+ nrd='0.29 / W' nrs='0.29 / W' sa=0 sb=0 sd=0 mult=miref m=miref
XM33 n5 n5 n4 vddh2 sky130_fd_pr__pfet_g5v0d10v5 L=10 W=3 nf=1 ad='int((nf+1)/2) * W/nf * 0.29' as='int((nf+2)/2) * W/nf * 0.29'
+ pd='2*int((nf+1)/2) * (W/nf + 0.29)' ps='2*int((nf+2)/2) * (W/nf + 0.29)' nrd='0.29 / W' nrs='0.29 / W'
+ sa=0 sb=0 sd=0 mult=2 m=2
XM34 nn2 nn2 nn1 gnd sky130_fd_pr__nfet_g5v0d10v5 L=l W=wn_iref nf=1 ad='int((nf+1)/2) * W/nf * 0.29'
+ as='int((nf+2)/2) * W/nf * 0.29' pd='2*int((nf+1)/2) * (W/nf + 0.29)' ps='2*int((nf+2)/2) * (W/nf + 0.29)'
+ nrd='0.29 / W' nrs='0.29 / W' sa=0 sb=0 sd=0 mult=miref m=miref
XM35 nn1 nn2 nn4 gnd sky130_fd_pr__nfet_g5v0d10v5 L=l W=wn_iref nf=1 ad='int((nf+1)/2) * W/nf * 0.29'
+ as='int((nf+2)/2) * W/nf * 0.29' pd='2*int((nf+1)/2) * (W/nf + 0.29)' ps='2*int((nf+2)/2) * (W/nf + 0.29)'
+ nrd='0.29 / W' nrs='0.29 / W' sa=0 sb=0 sd=0 mult=miref m=miref
XM36 nn4 nn1 net29 gnd sky130_fd_pr__nfet_g5v0d10v5 L=l W=wn_iref nf=1 ad='int((nf+1)/2) * W/nf * 0.29'
+ as='int((nf+2)/2) * W/nf * 0.29' pd='2*int((nf+1)/2) * (W/nf + 0.29)' ps='2*int((nf+2)/2) * (W/nf + 0.29)'
+ nrd='0.29 / W' nrs='0.29 / W' sa=0 sb=0 sd=0 mult=miref m=miref
XM37 net7 nn1 net8 net8 sky130_fd_pr__nfet_g5v0d10v5 L=l W=wn_iref nf=1 ad='int((nf+1)/2) * W/nf * 0.29'
+ as='int((nf+2)/2) * W/nf * 0.29' pd='2*int((nf+1)/2) * (W/nf + 0.29)' ps='2*int((nf+2)/2) * (W/nf + 0.29)'
+ nrd='0.29 / W' nrs='0.29 / W' sa=0 sb=0 sd=0 mult=miref2 m=miref2
XM38 vb2 n2 net9 vddh2 sky130_fd_pr__pfet_g5v0d10v5 L=l W=wp_iref nf=1 ad='int((nf+1)/2) * W/nf * 0.29'
+ as='int((nf+2)/2) * W/nf * 0.29' pd='2*int((nf+1)/2) * (W/nf + 0.29)' ps='2*int((nf+2)/2) * (W/nf + 0.29)'
+ nrd='0.29 / W' nrs='0.29 / W' sa=0 sb=0 sd=0 mult=miref2 m=miref2
XM41 net9 n1 vddh2 vddh2 sky130_fd_pr__pfet_g5v0d10v5 L=l W=wp_iref nf=1 ad='int((nf+1)/2) * W/nf * 0.29'
+ as='int((nf+2)/2) * W/nf * 0.29' pd='2*int((nf+1)/2) * (W/nf + 0.29)' ps='2*int((nf+2)/2) * (W/nf + 0.29)'
+ nrd='0.29 / W' nrs='0.29 / W' sa=0 sb=0 sd=0 mult=miref2 m=miref2
XM42 vb1 vb1 pvb1 vddh2 sky130_fd_pr__pfet_g5v0d10v5 L=l W=wp_bias nf=1 ad='int((nf+1)/2) * W/nf * 0.29'
+ as='int((nf+2)/2) * W/nf * 0.29' pd='2*int((nf+1)/2) * (W/nf + 0.29)' ps='2*int((nf+2)/2) * (W/nf + 0.29)'
+ nrd='0.29 / W' nrs='0.29 / W' sa=0 sb=0 sd=0 mult=mbias m=mbias
XM43 vb2 vb2 pvb2 net10 sky130_fd_pr__nfet_g5v0d10v5 L=l W=wn_bias nf=1 ad='int((nf+1)/2) * W/nf * 0.29'
+ as='int((nf+2)/2) * W/nf * 0.29' pd='2*int((nf+1)/2) * (W/nf + 0.29)' ps='2*int((nf+2)/2) * (W/nf + 0.29)'
+ nrd='0.29 / W' nrs='0.29 / W' sa=0 sb=0 sd=0 mult=mbias m=mbias
XM45 net35 vb2 IND gnd sky130_fd_pr__nfet_g5v0d10v5 L=l W=wn_fcm nf=1 ad='int((nf+1)/2) * W/nf * 0.29'
+ as='int((nf+2)/2) * W/nf * 0.29' pd='2*int((nf+1)/2) * (W/nf + 0.29)' ps='2*int((nf+2)/2) * (W/nf + 0.29)'
+ nrd='0.29 / W' nrs='0.29 / W' sa=0 sb=0 sd=0 mult=m_fcm m=m_fcm
XM48 IND vb1 net34 vddh2 sky130_fd_pr__pfet_g5v0d10v5 L=l W=wp_fcm nf=1 ad='int((nf+1)/2) * W/nf * 0.29'
+ as='int((nf+2)/2) * W/nf * 0.29' pd='2*int((nf+1)/2) * (W/nf + 0.29)' ps='2*int((nf+2)/2) * (W/nf + 0.29)'
+ nrd='0.29 / W' nrs='0.29 / W' sa=0 sb=0 sd=0 mult=m_fcm m=m_fcm
XM26 OUTPA vgn1 gnd gnd sky130_fd_pr__nfet_g5v0d10v5 L=l W={wn_sum*3} nf=1 ad='int((nf+1)/2) * W/nf * 0.29'
+ as='int((nf+2)/2) * W/nf * 0.29' pd='2*int((nf+1)/2) * (W/nf + 0.29)' ps='2*int((nf+2)/2) * (W/nf + 0.29)'
+ nrd='0.29 / W' nrs='0.29 / W' sa=0 sb=0 sd=0 mult=m_sum m=m_sum
**** begin user architecture code
.lib $::SKYWATER_MODELS/sky130.lib.spice tt



  .option wnflag=1
  .option safecurrents
  ********************Static Voltage Sources***************************
  Vddh vddh gnd dc 5.5

  *vina ina gnd sin({5.5/2} {5.5/2} 100k)
  *vinb inb gnd sin({5.5/2} {-5.5/2} 100k)

  .param vin_val=4.661
  *vin0 in[0] gnd dc vin_val
  *vin1 in[1] gnd dc vin_val
  *vin2 in[2] gnd dc vin_val
  *vin3 in[3] gnd dc vin_val
  *vin4 in[4] gnd dc vin_val
  ********************Dynamic Voltage Sources***************************
  *******Calculation**********
  .param base_f=100e3 base_t={1/base_f} base_th={base_t/2} base_d={base_th}
  .param b0_th={base_th} b0_t={b0_th*2}
  .param b1_th={b0_th*2} b1_t={b1_th*2}
  .param b2_th={b1_th*2} b2_t={b2_th*2}
  .param b3_th={b2_th*2} b3_t={b3_th*2}
  *******Signals**********
  .param vh=1.162 vl=1.044
*  vin0 in[0] gnd dc pulse(5.5 0 {base_d} 1n 1n {b0_th} {b0_t})
  vin0 in[0] gnd dc vl
  Vin1 in[1] gnd pulse({vh} {vl} {base_d} 1n 1n {b0_th} {b0_t})
  Vin2 in[2] gnd pulse({vh} {vl} {base_d} 1n 1n {b1_th} {b1_t})
  Vin3 in[3] gnd pulse({vh} {vl} {base_d} 1n 1n {b2_th} {b2_t})
  Vin4 in[4] gnd pulse({vh} {vl} {base_d} 1n 1n {b3_th} {b3_t})
  ********************Simulation Commands*****************************
  .control
     reset
     save all
     tran 1n 100u
     *dc vin0 -1 6.5 0.01
     *dc R2 1.9meg 2.1meg 10

     *ac dec 100 1 1e9

     let vout_mag =abs(v(out))
     let vout_phase_margin = phase(v(out))*180/pi + 180
     meas ac Aol find vout_mag at = 10
     meas ac UGF when vout_mag=1 fall=1
     meas ac PM find vout_phase_margin when vout_mag=1

     write op_amp_v3-tb.raw
     set wr_vecnames
     set wr_singlescale
     wrdata /home/yohanes/10-bit-DAC/simulations/op_amp_v3-tb.txt out load
     set appendwrite
*    quit 0
  .endc



**** end user architecture code
**.ends
.end
